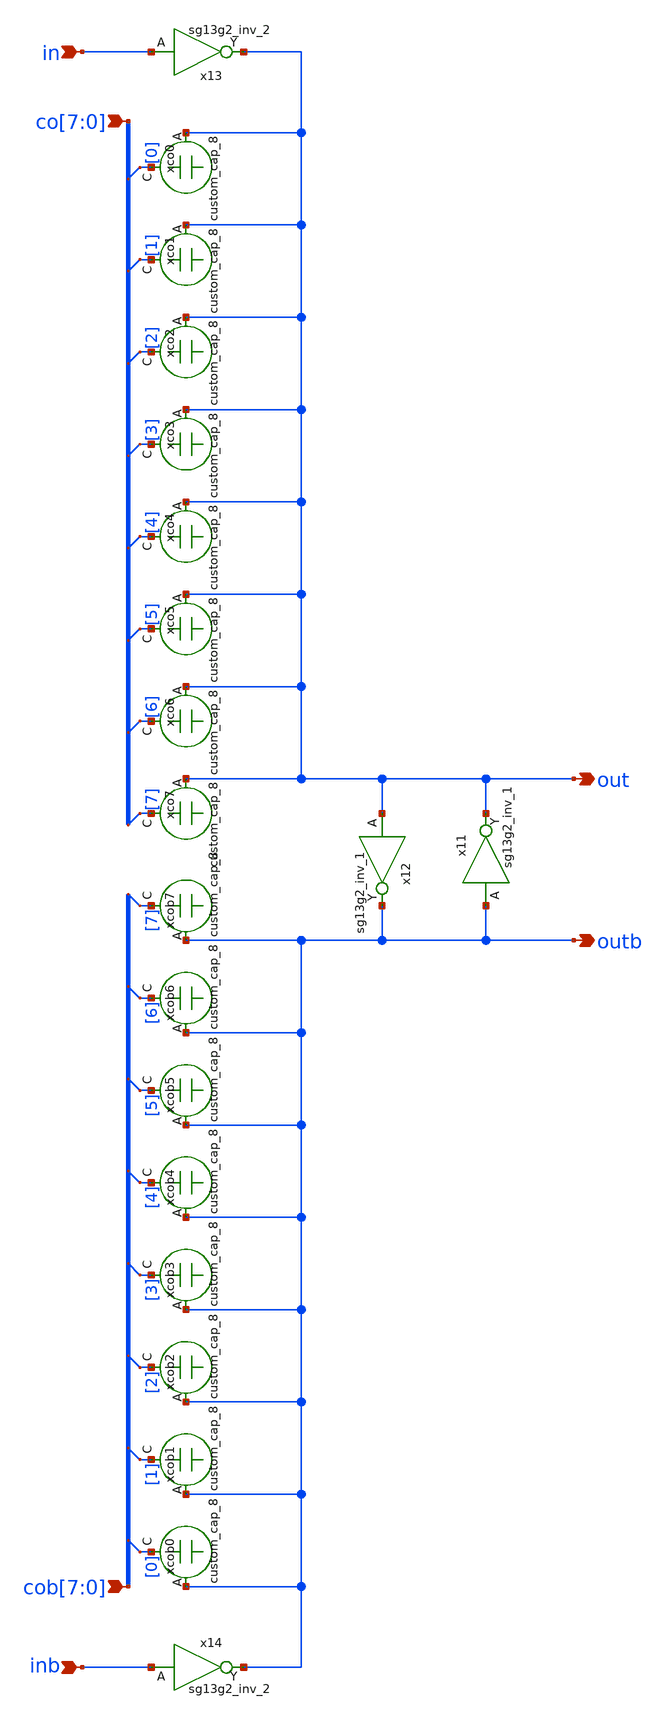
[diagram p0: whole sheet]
** sch_path: TPU5555-main/mdll/mixed_signal_design_blocks/clk_gen/src/delay_cell.sch
* IHP-GmbH/IHP-Open-PDK/ihp-sg13g2/libs.tech/xschem/sg13g2_stdcells/sg13g2_inv_2.sch:
* Copyright 2023 IHP PDK Authors
* Licensed under the Apache License, Version 2.0 (the "License");
**.subckt delay_cell in inb out outb co[7],co[6],co[5],co[4],co[3],co[2],co[1],co[0]
*+ cob[7],cob[6],cob[5],cob[4],cob[3],cob[2],cob[1],cob[0]
*.ipin in
*.ipin inb
*.opin out
*.opin outb
*.ipin co[7],co[6],co[5],co[4],co[3],co[2],co[1],co[0]
*.ipin cob[7],cob[6],cob[5],cob[4],cob[3],cob[2],cob[1],cob[0]
x13 out in VDD VSS sg13g2_inv_2
x14 outb inb VDD VSS sg13g2_inv_2
x11 out outb VDD VSS sg13g2_inv_1
x12 outb out VDD VSS sg13g2_inv_1
xco0 co[0] out VDD VSS custom_cap_8
* tap: co[7:0] --> co[0]
xco1 co[1] out VDD VSS custom_cap_8
* tap: co[7:0] --> co[1]
xco2 co[2] out VDD VSS custom_cap_8
* tap: co[7:0] --> co[2]
xco3 co[3] out VDD VSS custom_cap_8
* tap: co[7:0] --> co[3]
xco4 co[4] out VDD VSS custom_cap_8
* tap: co[7:0] --> co[4]
xco5 co[5] out VDD VSS custom_cap_8
* tap: co[7:0] --> co[5]
xco6 co[6] out VDD VSS custom_cap_8
* tap: co[7:0] --> co[6]
xco7 co[7] out VDD VSS custom_cap_8
* tap: co[7:0] --> co[7]
xcob0 cob[0] outb VDD VSS custom_cap_8
* tap: cob[7:0] --> cob[0]
xcob1 cob[1] outb VDD VSS custom_cap_8
* tap: cob[7:0] --> cob[1]
xcob2 cob[2] outb VDD VSS custom_cap_8
* tap: cob[7:0] --> cob[2]
xcob3 cob[3] outb VDD VSS custom_cap_8
* tap: cob[7:0] --> cob[3]
xcob4 cob[4] outb VDD VSS custom_cap_8
* tap: cob[7:0] --> cob[4]
xcob5 cob[5] outb VDD VSS custom_cap_8
* tap: cob[7:0] --> cob[5]
xcob6 cob[6] outb VDD VSS custom_cap_8
* tap: cob[7:0] --> cob[6]
xcob7 cob[7] outb VDD VSS custom_cap_8
* tap: cob[7:0] --> cob[7]
**.ends

* expanding   symbol:  sg13g2_inv_2.sym # of pins=2
** sym_path: sg13g2_inv_2.sym
** sch_path: sg13g2_inv_2.sch
.subckt sg13g2_inv_2 Y A VDD VSS
*.opin Y
*.ipin A
*.iopin VDD
*.iopin VSS
XM1 Y A VSS VSS sg13_lv_nmos w=1.48u l=130.00n ng=2 m=1 mm_ok=1
XM2 Y A VDD VDD sg13_lv_pmos w=2.24u l=130.00n ng=2 m=1 mm_ok=1
.ends


* expanding   symbol:  sg13g2_inv_1.sym # of pins=2
** sym_path: sg13g2_inv_1.sym
** sch_path: sg13g2_inv_1.sch
.subckt sg13g2_inv_1 Y A VDD VSS
*.opin Y
*.ipin A
*.iopin VDD
*.iopin VSS
XM1 Y A VSS VSS sg13_lv_nmos w=740.00n l=130.00n ng=1 m=1 mm_ok=1
XM2 Y A VDD VDD sg13_lv_pmos w=1.12u l=130.00n ng=1 m=1 mm_ok=1
.ends

.end
